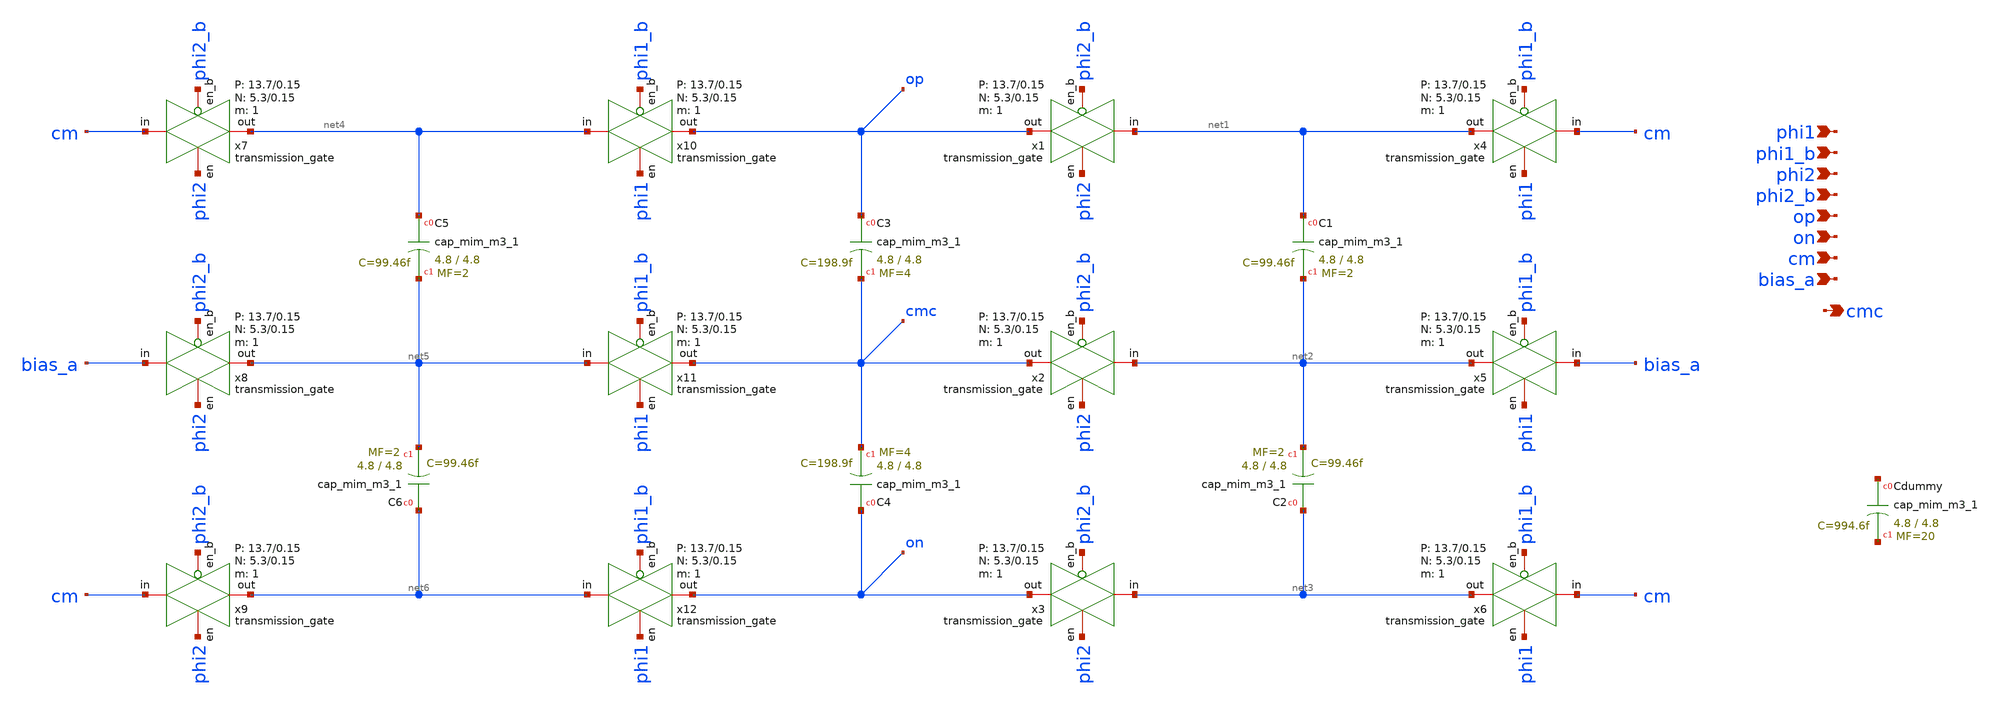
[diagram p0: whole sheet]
** sch_path: design/analog_modulator/schematic/sc_cmfb.sch
**.subckt sc_cmfb on cm bias_a op cmc phi2_b phi2 phi1_b phi1
*.ipin on
*.ipin cm
*.ipin bias_a
*.ipin op
*.opin cmc
*.ipin phi2_b
*.ipin phi2
*.ipin phi1_b
*.ipin phi1
XC3 op cmc sky130_fd_pr__cap_mim_m3_1 W=4.8 L=4.8 MF=4 m=4
XC4 on cmc sky130_fd_pr__cap_mim_m3_1 W=4.8 L=4.8 MF=4 m=4
x1 net1 op phi2 phi2_b VDD VSS 1 5.3 0.15 13.7 0.15 transmission_gate
x2 net2 cmc phi2 phi2_b VDD VSS 1 5.3 0.15 13.7 0.15 transmission_gate
x3 net3 on phi2 phi2_b VDD VSS 1 5.3 0.15 13.7 0.15 transmission_gate
x4 cm net1 phi1 phi1_b VDD VSS 1 5.3 0.15 13.7 0.15 transmission_gate
x5 bias_a net2 phi1 phi1_b VDD VSS 1 5.3 0.15 13.7 0.15 transmission_gate
x6 cm net3 phi1 phi1_b VDD VSS 1 5.3 0.15 13.7 0.15 transmission_gate
XC1 net1 net2 sky130_fd_pr__cap_mim_m3_1 W=4.8 L=4.8 MF=2 m=2
XC2 net3 net2 sky130_fd_pr__cap_mim_m3_1 W=4.8 L=4.8 MF=2 m=2
x7 cm net4 phi2 phi2_b VDD VSS 1 5.3 0.15 13.7 0.15 transmission_gate
x8 bias_a net5 phi2 phi2_b VDD VSS 1 5.3 0.15 13.7 0.15 transmission_gate
x9 cm net6 phi2 phi2_b VDD VSS 1 5.3 0.15 13.7 0.15 transmission_gate
x10 net4 op phi1 phi1_b VDD VSS 1 5.3 0.15 13.7 0.15 transmission_gate
x11 net5 cmc phi1 phi1_b VDD VSS 1 5.3 0.15 13.7 0.15 transmission_gate
x12 net6 on phi1 phi1_b VDD VSS 1 5.3 0.15 13.7 0.15 transmission_gate
XC5 net4 net5 sky130_fd_pr__cap_mim_m3_1 W=4.8 L=4.8 MF=2 m=2
XC6 net6 net5 sky130_fd_pr__cap_mim_m3_1 W=4.8 L=4.8 MF=2 m=2
XCdummy net7 net8 sky130_fd_pr__cap_mim_m3_1 W=4.8 L=4.8 MF=20 m=20
**.ends

* expanding   symbol:  transmission_gate.sym # of pins=4
** sym_path: design/analog_modulator/schematic/transmission_gate.sym
** sch_path: design/analog_modulator/schematic/transmission_gate.sch
.subckt transmission_gate in out en en_b VDD VSS N W_N L_N W_P L_P    N=1 W_N=5.3 L_N=0.15 W_P=13.7
+ L_P=0.15
*.iopin in
*.iopin out
*.ipin en
*.ipin en_b
XM1 out en in VSS sky130_fd_pr__nfet_01v8 L='L_N' W='W_N' nf=1 ad='int((nf+1)/2) * W/nf * 0.29' as='int((nf+2)/2) * W/nf * 0.29'
+ pd='2*int((nf+1)/2) * (W/nf + 0.29)' ps='2*int((nf+2)/2) * (W/nf + 0.29)' nrd='0.29 / W' nrs='0.29 / W'
+ sa=0 sb=0 sd=0 mult='N' m='N'
XM2 out en_b in VDD sky130_fd_pr__pfet_01v8 L='L_P' W='W_P' nf=1 ad='int((nf+1)/2) * W/nf * 0.29' as='int((nf+2)/2) * W/nf * 0.29'
+ pd='2*int((nf+1)/2) * (W/nf + 0.29)' ps='2*int((nf+2)/2) * (W/nf + 0.29)' nrd='0.29 / W' nrs='0.29 / W'
+ sa=0 sb=0 sd=0 mult='N' m='N'
.ends

.end
